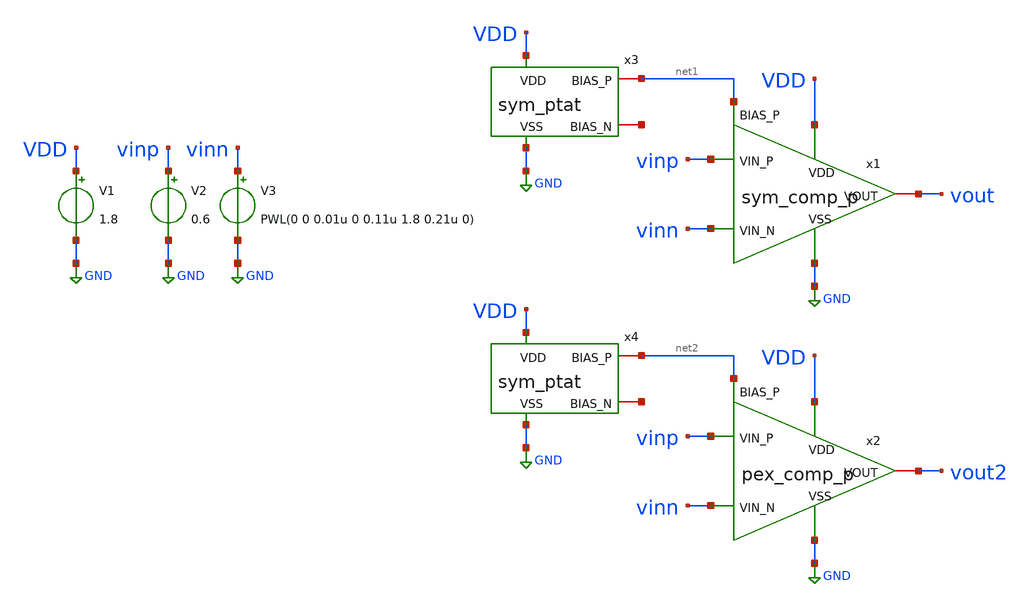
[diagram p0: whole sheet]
** sch_path: schem/tb/tb_comp_p.sch
**.subckt tb_comp_p
V1 VDD GND 1.8
V2 vinp GND 0.6
V3 vinn GND PWL(0 0 0.01u 0 0.11u 1.8 0.21u 0)
x1 VDD GND net1 vout vinp vinn sym_comp_p
x2 VDD GND net2 vout2 vinp vinn comp_p
x3 VDD GND net1 net3 sym_ptat
x4 VDD GND net2 net4 sym_ptat
**** begin user architecture code


.include /home/zhixuan/projects/fyp_vco/magic/ip/comp_p/comp_p.spice
.lib /usr/local/share/pdk/sky130A/libs.tech/ngspice/sky130.lib.spice tt

.tran 0.1n 0.21u
.save all

.control
    run
    plot vinn vinp vout vout2

    echo "vinn vinp vout2" > /home/zhixuan/projects/fyp_vco/schem/tb/compp_tb_out1.txt
    print col vinn vinp vout2 >> /home/zhixuan/projects/fyp_vco/schem/tb/compp_tb_out1.txt
.endc

.end


**** end user architecture code
**.ends

* expanding   symbol:  /home/zhixuan/projects/fyp_vco/schem/symbol_repo/sym_comp_p.sym # of pins=6
** sym_path: schem/symbol_repo/sym_comp_p.sym
** sch_path: schem/symbol_repo/sym_comp_p.sch
.subckt sym_comp_p VDD VSS BIAS_P VOUT VIN_P VIN_N
*.ipin VDD
*.ipin VSS
*.ipin BIAS_P
*.ipin VIN_N
*.ipin VIN_P
*.iopin VOUT
XMN_cs_l net2 net1 VSS VSS sky130_fd_pr__nfet_01v8 L=0.15 W=1 nf=1 ad='int((1 + 1)/2) * 1 / 1 * 0.29'
+ as='int((1 + 2)/2) * 1 / 1 * 0.29' pd='2*int((1 + 1)/2) * (1 / 1 + 0.29)' ps='2*int((1 + 2)/2) * (1 / 1 + 0.29)'
+ nrd='0.29 / 1 ' nrs='0.29 / 1 ' sa=0 sb=0 sd=0 mult=1 m=1
XMP_tail net4 BIAS_P VDD VDD sky130_fd_pr__pfet_01v8 L=0.75 W=2 nf=5 ad='int((5 + 1)/2) * 2 / 5 * 0.29'
+ as='int((5 + 2)/2) * 2 / 5 * 0.29' pd='2*int((5 + 1)/2) * (2 / 5 + 0.29)' ps='2*int((5 + 2)/2) * (2 / 5 + 0.29)'
+ nrd='0.29 / 2 ' nrs='0.29 / 2 ' sa=0 sb=0 sd=0 mult=1 m=1
XMP_vinn net1 VIN_N net4 VDD sky130_fd_pr__pfet_01v8 L=0.5 W=2.5 nf=2 ad='int((2 + 1)/2) * 2.5 / 2 * 0.29'
+ as='int((2 + 2)/2) * 2.5 / 2 * 0.29' pd='2*int((2 + 1)/2) * (2.5 / 2 + 0.29)' ps='2*int((2 + 2)/2) * (2.5 / 2 + 0.29)'
+ nrd='0.29 / 2.5 ' nrs='0.29 / 2.5 ' sa=0 sb=0 sd=0 mult=1 m=1
XMP_vinp net2 VIN_P net4 VDD sky130_fd_pr__pfet_01v8 L=0.5 W=2.5 nf=2 ad='int((2 + 1)/2) * 2.5 / 2 * 0.29'
+ as='int((2 + 2)/2) * 2.5 / 2 * 0.29' pd='2*int((2 + 1)/2) * (2.5 / 2 + 0.29)' ps='2*int((2 + 2)/2) * (2.5 / 2 + 0.29)'
+ nrd='0.29 / 2.5 ' nrs='0.29 / 2.5 ' sa=0 sb=0 sd=0 mult=1 m=1
XMN_diode_l net1 net1 VSS VSS sky130_fd_pr__nfet_01v8 L=0.15 W=1 nf=1 ad='int((1 + 1)/2) * 1 / 1 * 0.29'
+ as='int((1 + 2)/2) * 1 / 1 * 0.29' pd='2*int((1 + 1)/2) * (1 / 1 + 0.29)' ps='2*int((1 + 2)/2) * (1 / 1 + 0.29)'
+ nrd='0.29 / 1 ' nrs='0.29 / 1 ' sa=0 sb=0 sd=0 mult=1 m=1
XMN_diode_r net2 net2 VSS VSS sky130_fd_pr__nfet_01v8 L=0.15 W=1 nf=1 ad='int((1 + 1)/2) * 1 / 1 * 0.29'
+ as='int((1 + 2)/2) * 1 / 1 * 0.29' pd='2*int((1 + 1)/2) * (1 / 1 + 0.29)' ps='2*int((1 + 2)/2) * (1 / 1 + 0.29)'
+ nrd='0.29 / 1 ' nrs='0.29 / 1 ' sa=0 sb=0 sd=0 mult=1 m=1
XMN_cs_r net1 net2 VSS VSS sky130_fd_pr__nfet_01v8 L=0.15 W=1 nf=1 ad='int((1 + 1)/2) * 1 / 1 * 0.29'
+ as='int((1 + 2)/2) * 1 / 1 * 0.29' pd='2*int((1 + 1)/2) * (1 / 1 + 0.29)' ps='2*int((1 + 2)/2) * (1 / 1 + 0.29)'
+ nrd='0.29 / 1 ' nrs='0.29 / 1 ' sa=0 sb=0 sd=0 mult=1 m=1
XMN_latch_l net5 net1 VSS VSS sky130_fd_pr__nfet_01v8 L=0.15 W=0.5 nf=1 ad='int((1 + 1)/2) * 0.5 / 1 * 0.29'
+ as='int((1 + 2)/2) * 0.5 / 1 * 0.29' pd='2*int((1 + 1)/2) * (0.5 / 1 + 0.29)' ps='2*int((1 + 2)/2) * (0.5 / 1 + 0.29)'
+ nrd='0.29 / 0.5 ' nrs='0.29 / 0.5 ' sa=0 sb=0 sd=0 mult=1 m=1
XMN_latch_r VOUT net2 VSS VSS sky130_fd_pr__nfet_01v8 L=0.15 W=0.5 nf=1 ad='int((1 + 1)/2) * 0.5 / 1 * 0.29'
+ as='int((1 + 2)/2) * 0.5 / 1 * 0.29' pd='2*int((1 + 1)/2) * (0.5 / 1 + 0.29)' ps='2*int((1 + 2)/2) * (0.5 / 1 + 0.29)'
+ nrd='0.29 / 0.5 ' nrs='0.29 / 0.5 ' sa=0 sb=0 sd=0 mult=1 m=1
XMP_diode_l net3 net3 VDD VDD sky130_fd_pr__pfet_01v8 L=0.15 W=0.5 nf=1 ad='int((1 + 1)/2) * 0.5 / 1 * 0.29'
+ as='int((1 + 2)/2) * 0.5 / 1 * 0.29' pd='2*int((1 + 1)/2) * (0.5 / 1 + 0.29)' ps='2*int((1 + 2)/2) * (0.5 / 1 + 0.29)'
+ nrd='0.29 / 0.5 ' nrs='0.29 / 0.5 ' sa=0 sb=0 sd=0 mult=1 m=1
XMP_latch_r VOUT net3 VDD VDD sky130_fd_pr__pfet_01v8 L=0.15 W=0.5 nf=1 ad='int((1 + 1)/2) * 0.5 / 1 * 0.29'
+ as='int((1 + 2)/2) * 0.5 / 1 * 0.29' pd='2*int((1 + 1)/2) * (0.5 / 1 + 0.29)' ps='2*int((1 + 2)/2) * (0.5 / 1 + 0.29)'
+ nrd='0.29 / 0.5 ' nrs='0.29 / 0.5 ' sa=0 sb=0 sd=0 mult=1 m=1
XMP_lim net5 net5 net3 VDD sky130_fd_pr__pfet_01v8 L=0.15 W=0.5 nf=1 ad='int((1 + 1)/2) * 0.5 / 1 * 0.29'
+ as='int((1 + 2)/2) * 0.5 / 1 * 0.29' pd='2*int((1 + 1)/2) * (0.5 / 1 + 0.29)' ps='2*int((1 + 2)/2) * (0.5 / 1 + 0.29)'
+ nrd='0.29 / 0.5 ' nrs='0.29 / 0.5 ' sa=0 sb=0 sd=0 mult=1 m=1
.ends


* expanding   symbol:  /home/zhixuan/projects/fyp_vco/schem/symbol_repo/sym_ptat.sym # of pins=4
** sym_path: schem/symbol_repo/sym_ptat.sym
** sch_path: schem/symbol_repo/sym_ptat.sch
.subckt sym_ptat VDD VSS BIAS_P BIAS_N
*.ipin VDD
*.ipin VSS
*.iopin BIAS_P
*.iopin BIAS_N
XMN_ptat2 net6 net1 net2 VSS sky130_fd_pr__nfet_01v8 L=0.5 W=2 nf=2 ad='int((2 + 1)/2) * 2 / 2 * 0.29'
+ as='int((2 + 2)/2) * 2 / 2 * 0.29' pd='2*int((2 + 1)/2) * (2 / 2 + 0.29)' ps='2*int((2 + 2)/2) * (2 / 2 + 0.29)'
+ nrd='0.29 / 2 ' nrs='0.29 / 2 ' sa=0 sb=0 sd=0 mult=1 m=1
XMP_diode1 net3 BIAS_P VDD VDD sky130_fd_pr__pfet_01v8 L=0.5 W=2 nf=2 ad='int((2 + 1)/2) * 2 / 2 * 0.29'
+ as='int((2 + 2)/2) * 2 / 2 * 0.29' pd='2*int((2 + 1)/2) * (2 / 2 + 0.29)' ps='2*int((2 + 2)/2) * (2 / 2 + 0.29)'
+ nrd='0.29 / 2 ' nrs='0.29 / 2 ' sa=0 sb=0 sd=0 mult=1 m=1
XMP_mir1_l net4 BIAS_P VDD VDD sky130_fd_pr__pfet_01v8 L=0.5 W=2 nf=2 ad='int((2 + 1)/2) * 2 / 2 * 0.29'
+ as='int((2 + 2)/2) * 2 / 2 * 0.29' pd='2*int((2 + 1)/2) * (2 / 2 + 0.29)' ps='2*int((2 + 2)/2) * (2 / 2 + 0.29)'
+ nrd='0.29 / 2 ' nrs='0.29 / 2 ' sa=0 sb=0 sd=0 mult=1 m=1
XMN_diode2 net5 net1 VSS VSS sky130_fd_pr__nfet_01v8 L=0.5 W=2 nf=4 ad='int((4 + 1)/2) * 2 / 4 * 0.29'
+ as='int((4 + 2)/2) * 2 / 4 * 0.29' pd='2*int((4 + 1)/2) * (2 / 4 + 0.29)' ps='2*int((4 + 2)/2) * (2 / 4 + 0.29)'
+ nrd='0.29 / 2 ' nrs='0.29 / 2 ' sa=0 sb=0 sd=0 mult=1 m=1
XMP_inv BIAS_N BIAS_P VDD VDD sky130_fd_pr__pfet_01v8 L=0.75 W=2 nf=5 ad='int((5 + 1)/2) * 2 / 5 * 0.29'
+ as='int((5 + 2)/2) * 2 / 5 * 0.29' pd='2*int((5 + 1)/2) * (2 / 5 + 0.29)' ps='2*int((5 + 2)/2) * (2 / 5 + 0.29)'
+ nrd='0.29 / 2 ' nrs='0.29 / 2 ' sa=0 sb=0 sd=0 mult=1 m=1
XMP_diode2 BIAS_P BIAS_P net3 VDD sky130_fd_pr__pfet_01v8 L=0.5 W=2 nf=2 ad='int((2 + 1)/2) * 2 / 2 * 0.29'
+ as='int((2 + 2)/2) * 2 / 2 * 0.29' pd='2*int((2 + 1)/2) * (2 / 2 + 0.29)' ps='2*int((2 + 2)/2) * (2 / 2 + 0.29)'
+ nrd='0.29 / 2 ' nrs='0.29 / 2 ' sa=0 sb=0 sd=0 mult=1 m=1
XMP_mir2_l net1 BIAS_P net4 VDD sky130_fd_pr__pfet_01v8 L=0.5 W=2 nf=2 ad='int((2 + 1)/2) * 2 / 2 * 0.29'
+ as='int((2 + 2)/2) * 2 / 2 * 0.29' pd='2*int((2 + 1)/2) * (2 / 2 + 0.29)' ps='2*int((2 + 2)/2) * (2 / 2 + 0.29)'
+ nrd='0.29 / 2 ' nrs='0.29 / 2 ' sa=0 sb=0 sd=0 mult=1 m=1
XMN_ptat1 BIAS_P net1 net6 VSS sky130_fd_pr__nfet_01v8 L=0.5 W=2 nf=2 ad='int((2 + 1)/2) * 2 / 2 * 0.29'
+ as='int((2 + 2)/2) * 2 / 2 * 0.29' pd='2*int((2 + 1)/2) * (2 / 2 + 0.29)' ps='2*int((2 + 2)/2) * (2 / 2 + 0.29)'
+ nrd='0.29 / 2 ' nrs='0.29 / 2 ' sa=0 sb=0 sd=0 mult=1 m=1
XMN_diode1 net1 net1 net5 VSS sky130_fd_pr__nfet_01v8 L=0.5 W=2 nf=4 ad='int((4 + 1)/2) * 2 / 4 * 0.29'
+ as='int((4 + 2)/2) * 2 / 4 * 0.29' pd='2*int((4 + 1)/2) * (2 / 4 + 0.29)' ps='2*int((4 + 2)/2) * (2 / 4 + 0.29)'
+ nrd='0.29 / 2 ' nrs='0.29 / 2 ' sa=0 sb=0 sd=0 mult=1 m=1
XMN_inv BIAS_N BIAS_N VSS VSS sky130_fd_pr__nfet_01v8 L=0.75 W=2.5 nf=2 ad='int((2 + 1)/2) * 2.5 / 2 * 0.29'
+ as='int((2 + 2)/2) * 2.5 / 2 * 0.29' pd='2*int((2 + 1)/2) * (2.5 / 2 + 0.29)' ps='2*int((2 + 2)/2) * (2.5 / 2 + 0.29)'
+ nrd='0.29 / 2.5 ' nrs='0.29 / 2.5 ' sa=0 sb=0 sd=0 mult=1 m=1
XR1 VSS net2 VSS sky130_fd_pr__res_xhigh_po_0p35 L=2.8 mult=1 m=1
XMP_startup net1 VSS VDD VDD sky130_fd_pr__pfet_01v8 L=13 W=1 nf=1 ad='int((1 + 1)/2) * 1 / 1 * 0.29'
+ as='int((1 + 2)/2) * 1 / 1 * 0.29' pd='2*int((1 + 1)/2) * (1 / 1 + 0.29)' ps='2*int((1 + 2)/2) * (1 / 1 + 0.29)'
+ nrd='0.29 / 1 ' nrs='0.29 / 1 ' sa=0 sb=0 sd=0 mult=1 m=1
XMN_diode3 net7 net1 VSS VSS sky130_fd_pr__nfet_01v8 L=0.5 W=2 nf=4 ad='int((4 + 1)/2) * 2 / 4 * 0.29'
+ as='int((4 + 2)/2) * 2 / 4 * 0.29' pd='2*int((4 + 1)/2) * (2 / 4 + 0.29)' ps='2*int((4 + 2)/2) * (2 / 4 + 0.29)'
+ nrd='0.29 / 2 ' nrs='0.29 / 2 ' sa=0 sb=0 sd=0 mult=1 m=1
XMN_diode4 net1 net1 net7 VSS sky130_fd_pr__nfet_01v8 L=0.5 W=2 nf=4 ad='int((4 + 1)/2) * 2 / 4 * 0.29'
+ as='int((4 + 2)/2) * 2 / 4 * 0.29' pd='2*int((4 + 1)/2) * (2 / 4 + 0.29)' ps='2*int((4 + 2)/2) * (2 / 4 + 0.29)'
+ nrd='0.29 / 2 ' nrs='0.29 / 2 ' sa=0 sb=0 sd=0 mult=1 m=1
.ends

.GLOBAL GND
.end
